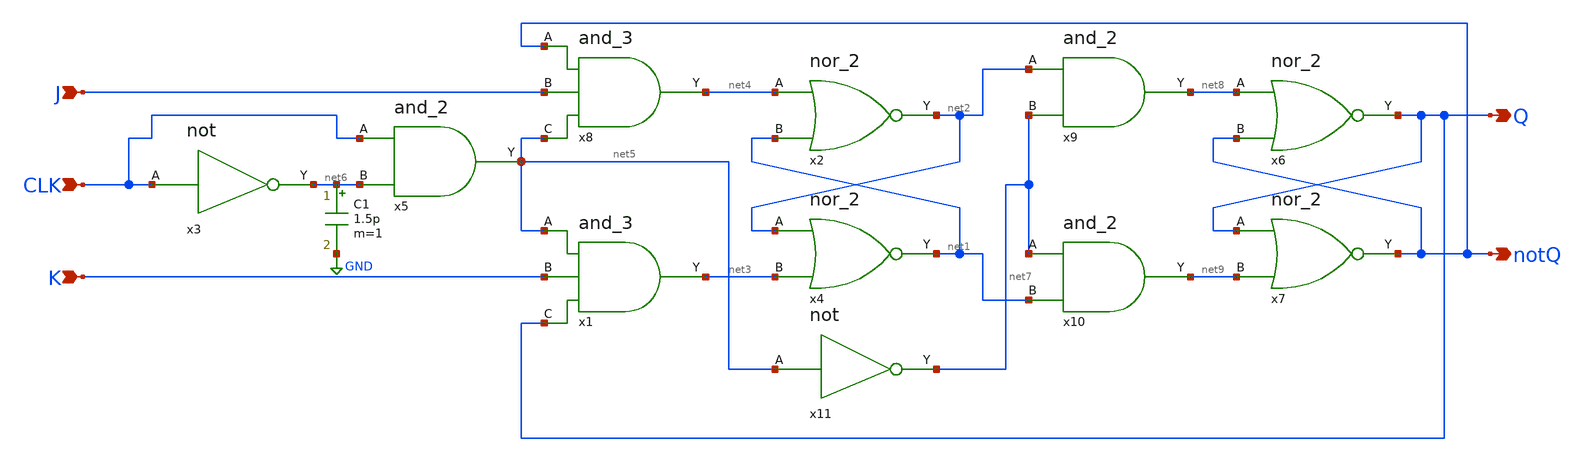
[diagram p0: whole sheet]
** sch_path: Circuiti/latches_sch_sym/jk_latch_ms.sch
**.subckt jk_latch_ms K CLK Q notQ J
*.ipin K
*.ipin CLK
*.opin Q
*.opin notQ
*.ipin J
x3 CLK net6 not
x5 CLK net5 net6 and_2
x1 net5 net3 K Q and_3
x2 net4 net2 net1 nor_2
x4 net2 net1 net3 nor_2
x6 net8 Q notQ nor_2
x7 Q notQ net9 nor_2
x8 notQ net4 J net5 and_3
C1 net6 GND 1.5p m=1
x9 net2 net8 net7 and_2
x10 net7 net9 net1 and_2
x11 net5 net7 not
**.ends

* expanding   symbol:  /home/matteo/Documenti/tesi/Circuiti/logic_gates_sch_sym/not.sym # of pins=2
** sym_path: Circuiti/logic_gates_sch_sym/not.sym
** sch_path: Circuiti/logic_gates_sch_sym/not.sch
.subckt not A Y
*.ipin A
*.opin Y
XM1 Y A GND GND sky130_fd_pr__nfet_01v8 L=0.45 W=1 nf=1 ad='int((nf+1)/2) * W/nf * 0.29' as='int((nf+2)/2) * W/nf * 0.29'
+ pd='2*int((nf+1)/2) * (W/nf + 0.29)' ps='2*int((nf+2)/2) * (W/nf + 0.29)' nrd='0.29 / W' nrs='0.29 / W'
+ sa=0 sb=0 sd=0 mult=1 m=1
XM2 Y A Vdd VDD sky130_fd_pr__pfet_01v8 L=0.45 W=4.8 nf=1 ad='int((nf+1)/2) * W/nf * 0.29' as='int((nf+2)/2) * W/nf * 0.29'
+ pd='2*int((nf+1)/2) * (W/nf + 0.29)' ps='2*int((nf+2)/2) * (W/nf + 0.29)' nrd='0.29 / W' nrs='0.29 / W'
+ sa=0 sb=0 sd=0 mult=1 m=1
.ends


* expanding   symbol:  /home/matteo/Documenti/tesi/Circuiti/logic_gates_sch_sym/and_2.sym # of
*+ pins=3
** sym_path: Circuiti/logic_gates_sch_sym/and_2.sym
** sch_path: Circuiti/logic_gates_sch_sym/and_2.sch
.subckt and_2 A Y B
*.ipin B
*.ipin A
*.opin Y
x1 A net1 B nand_2
x2 net1 Y not
.ends


* expanding   symbol:  /home/matteo/Documenti/tesi/Circuiti/logic_gates_sch_sym/and_3.sym # of
*+ pins=4
** sym_path: Circuiti/logic_gates_sch_sym/and_3.sym
** sch_path: Circuiti/logic_gates_sch_sym/and_3.sch
.subckt and_3 A Y B C
*.ipin A
*.ipin B
*.ipin C
*.opin Y
x1 A Y net1 and_2
x2 B net1 C and_2
.ends


* expanding   symbol:  /home/matteo/Documenti/tesi/Circuiti/logic_gates_sch_sym/nor_2.sym # of
*+ pins=3
** sym_path: Circuiti/logic_gates_sch_sym/nor_2.sym
** sch_path: Circuiti/logic_gates_sch_sym/nor_2.sch
.subckt nor_2 A Y B
*.opin Y
*.ipin A
*.ipin B
XM1 Y B GND GND sky130_fd_pr__nfet_01v8 L=0.45 W=1 nf=1 ad='int((nf+1)/2) * W/nf * 0.29' as='int((nf+2)/2) * W/nf * 0.29'
+ pd='2*int((nf+1)/2) * (W/nf + 0.29)' ps='2*int((nf+2)/2) * (W/nf + 0.29)' nrd='0.29 / W' nrs='0.29 / W'
+ sa=0 sb=0 sd=0 mult=1 m=1
XM3 Y B net1 VDD sky130_fd_pr__pfet_01v8 L=0.15 W=4.8 nf=1 ad='int((nf+1)/2) * W/nf * 0.29' as='int((nf+2)/2) * W/nf * 0.29'
+ pd='2*int((nf+1)/2) * (W/nf + 0.29)' ps='2*int((nf+2)/2) * (W/nf + 0.29)' nrd='0.29 / W' nrs='0.29 / W'
+ sa=0 sb=0 sd=0 mult=1 m=1
XM4 net1 A Vdd VDD sky130_fd_pr__pfet_01v8 L=0.15 W=4.8 nf=1 ad='int((nf+1)/2) * W/nf * 0.29' as='int((nf+2)/2) * W/nf * 0.29'
+ pd='2*int((nf+1)/2) * (W/nf + 0.29)' ps='2*int((nf+2)/2) * (W/nf + 0.29)' nrd='0.29 / W' nrs='0.29 / W'
+ sa=0 sb=0 sd=0 mult=1 m=1
XM2 Y A GND GND sky130_fd_pr__nfet_01v8 L=0.45 W=1 nf=1 ad='int((nf+1)/2) * W/nf * 0.29' as='int((nf+2)/2) * W/nf * 0.29'
+ pd='2*int((nf+1)/2) * (W/nf + 0.29)' ps='2*int((nf+2)/2) * (W/nf + 0.29)' nrd='0.29 / W' nrs='0.29 / W'
+ sa=0 sb=0 sd=0 mult=1 m=1
.ends


* expanding   symbol:  /home/matteo/Documenti/tesi/Circuiti/logic_gates_sch_sym/nand_2.sym # of
*+ pins=3
** sym_path: Circuiti/logic_gates_sch_sym/nand_2.sym
** sch_path: Circuiti/logic_gates_sch_sym/nand_2.sch
.subckt nand_2 A Y B
*.ipin A
*.ipin B
*.opin Y
XM1 Y A net1 GND sky130_fd_pr__nfet_01v8 L=0.15 W=1 nf=1 ad='int((nf+1)/2) * W/nf * 0.29' as='int((nf+2)/2) * W/nf * 0.29'
+ pd='2*int((nf+1)/2) * (W/nf + 0.29)' ps='2*int((nf+2)/2) * (W/nf + 0.29)' nrd='0.29 / W' nrs='0.29 / W'
+ sa=0 sb=0 sd=0 mult=1 m=1
XM3 Y B Vdd VDD sky130_fd_pr__pfet_01v8 L=0.45 W=4.8 nf=1 ad='int((nf+1)/2) * W/nf * 0.29' as='int((nf+2)/2) * W/nf * 0.29'
+ pd='2*int((nf+1)/2) * (W/nf + 0.29)' ps='2*int((nf+2)/2) * (W/nf + 0.29)' nrd='0.29 / W' nrs='0.29 / W'
+ sa=0 sb=0 sd=0 mult=1 m=1
XM4 Y A Vdd VDD sky130_fd_pr__pfet_01v8 L=0.45 W=4.8 nf=1 ad='int((nf+1)/2) * W/nf * 0.29' as='int((nf+2)/2) * W/nf * 0.29'
+ pd='2*int((nf+1)/2) * (W/nf + 0.29)' ps='2*int((nf+2)/2) * (W/nf + 0.29)' nrd='0.29 / W' nrs='0.29 / W'
+ sa=0 sb=0 sd=0 mult=1 m=1
XM2 net1 B GND GND sky130_fd_pr__nfet_01v8 L=0.15 W=1 nf=1 ad='int((nf+1)/2) * W/nf * 0.29' as='int((nf+2)/2) * W/nf * 0.29'
+ pd='2*int((nf+1)/2) * (W/nf + 0.29)' ps='2*int((nf+2)/2) * (W/nf + 0.29)' nrd='0.29 / W' nrs='0.29 / W'
+ sa=0 sb=0 sd=0 mult=1 m=1
.ends

.GLOBAL GND
.GLOBAL Vdd
.end
